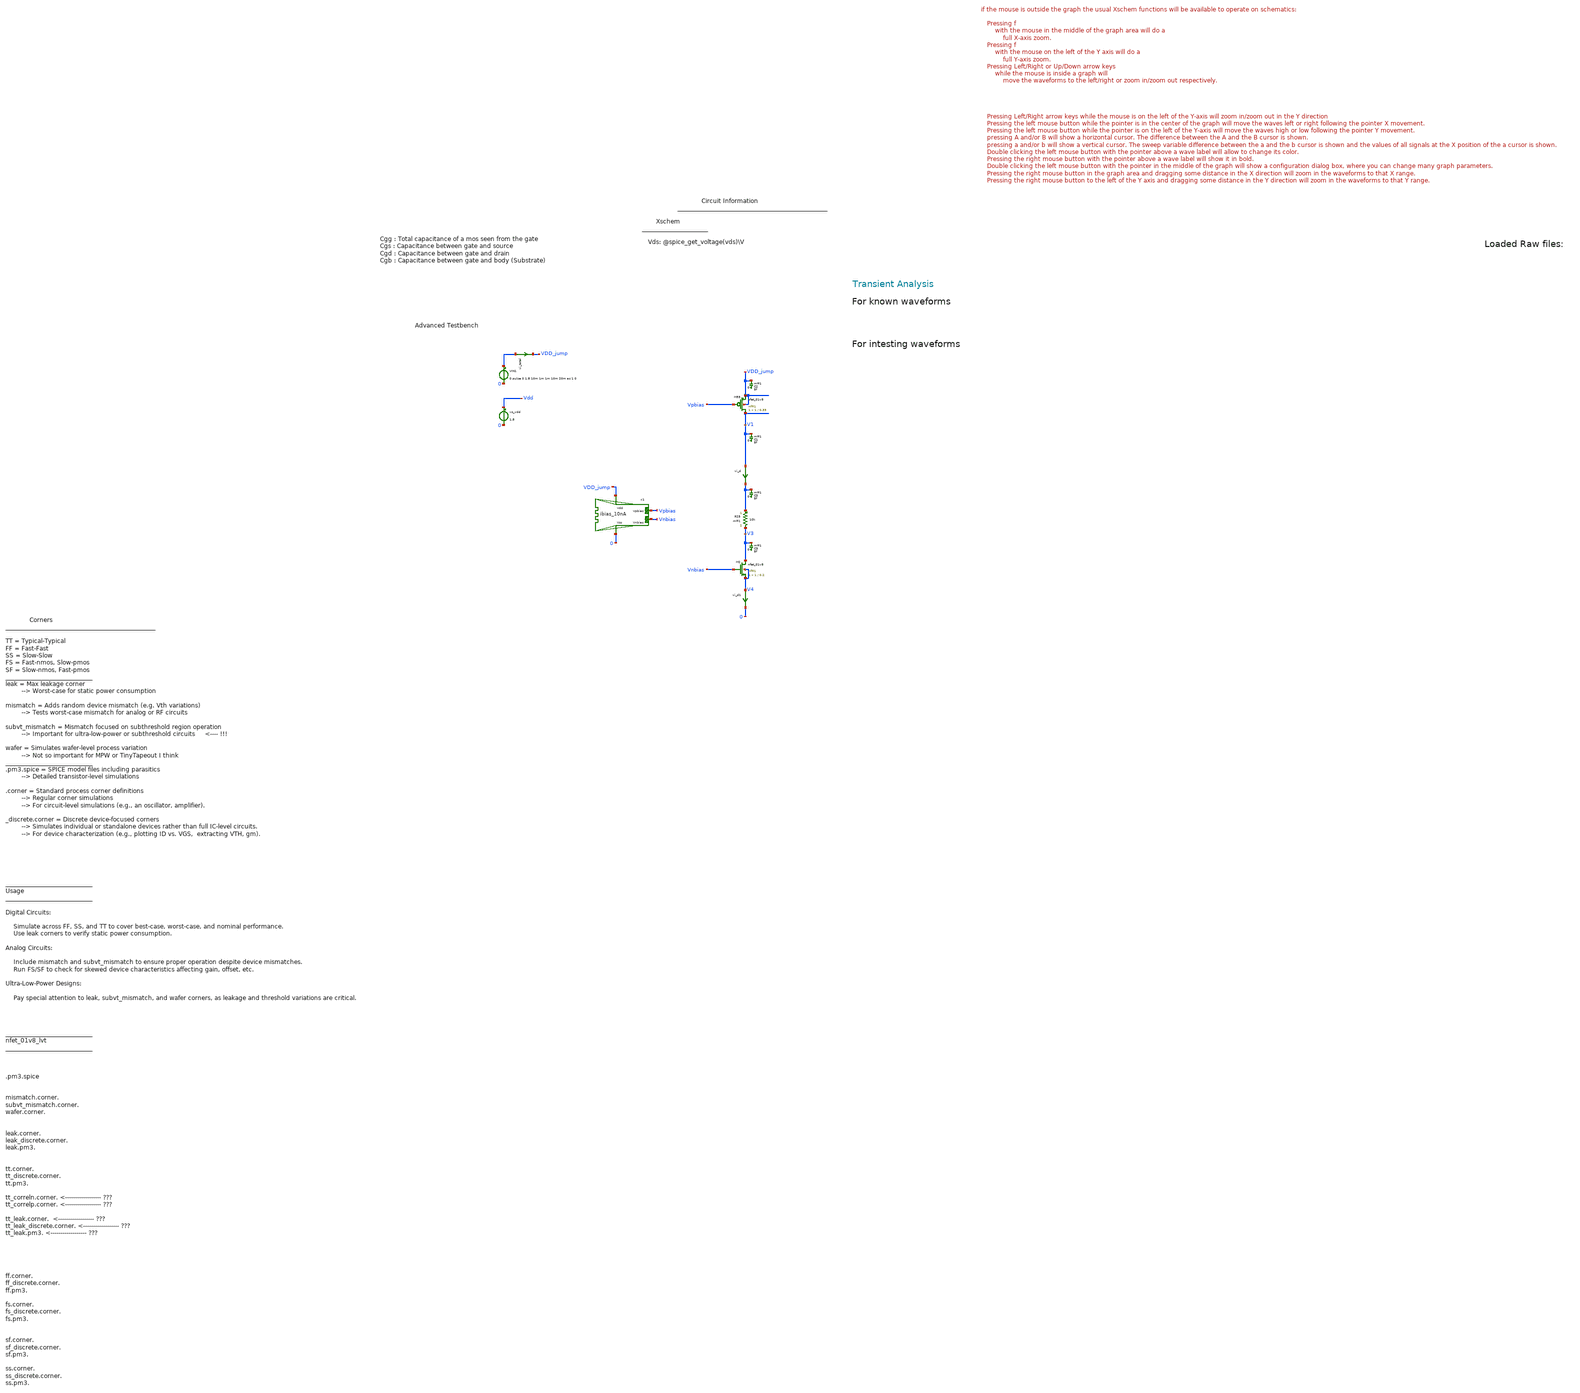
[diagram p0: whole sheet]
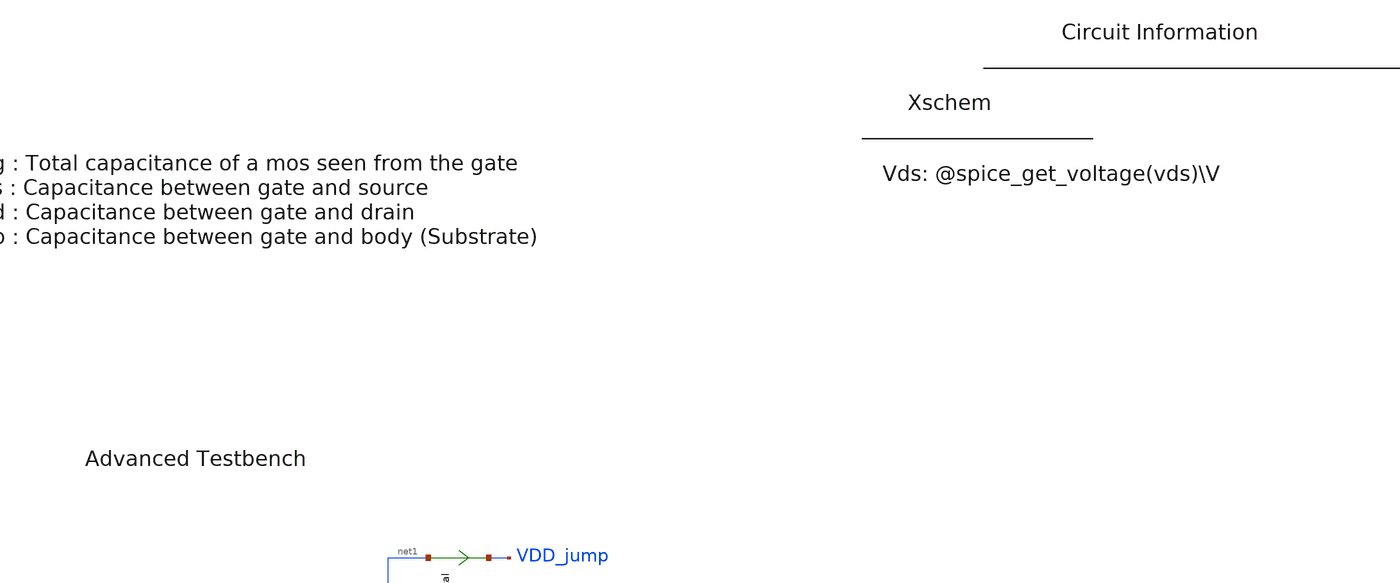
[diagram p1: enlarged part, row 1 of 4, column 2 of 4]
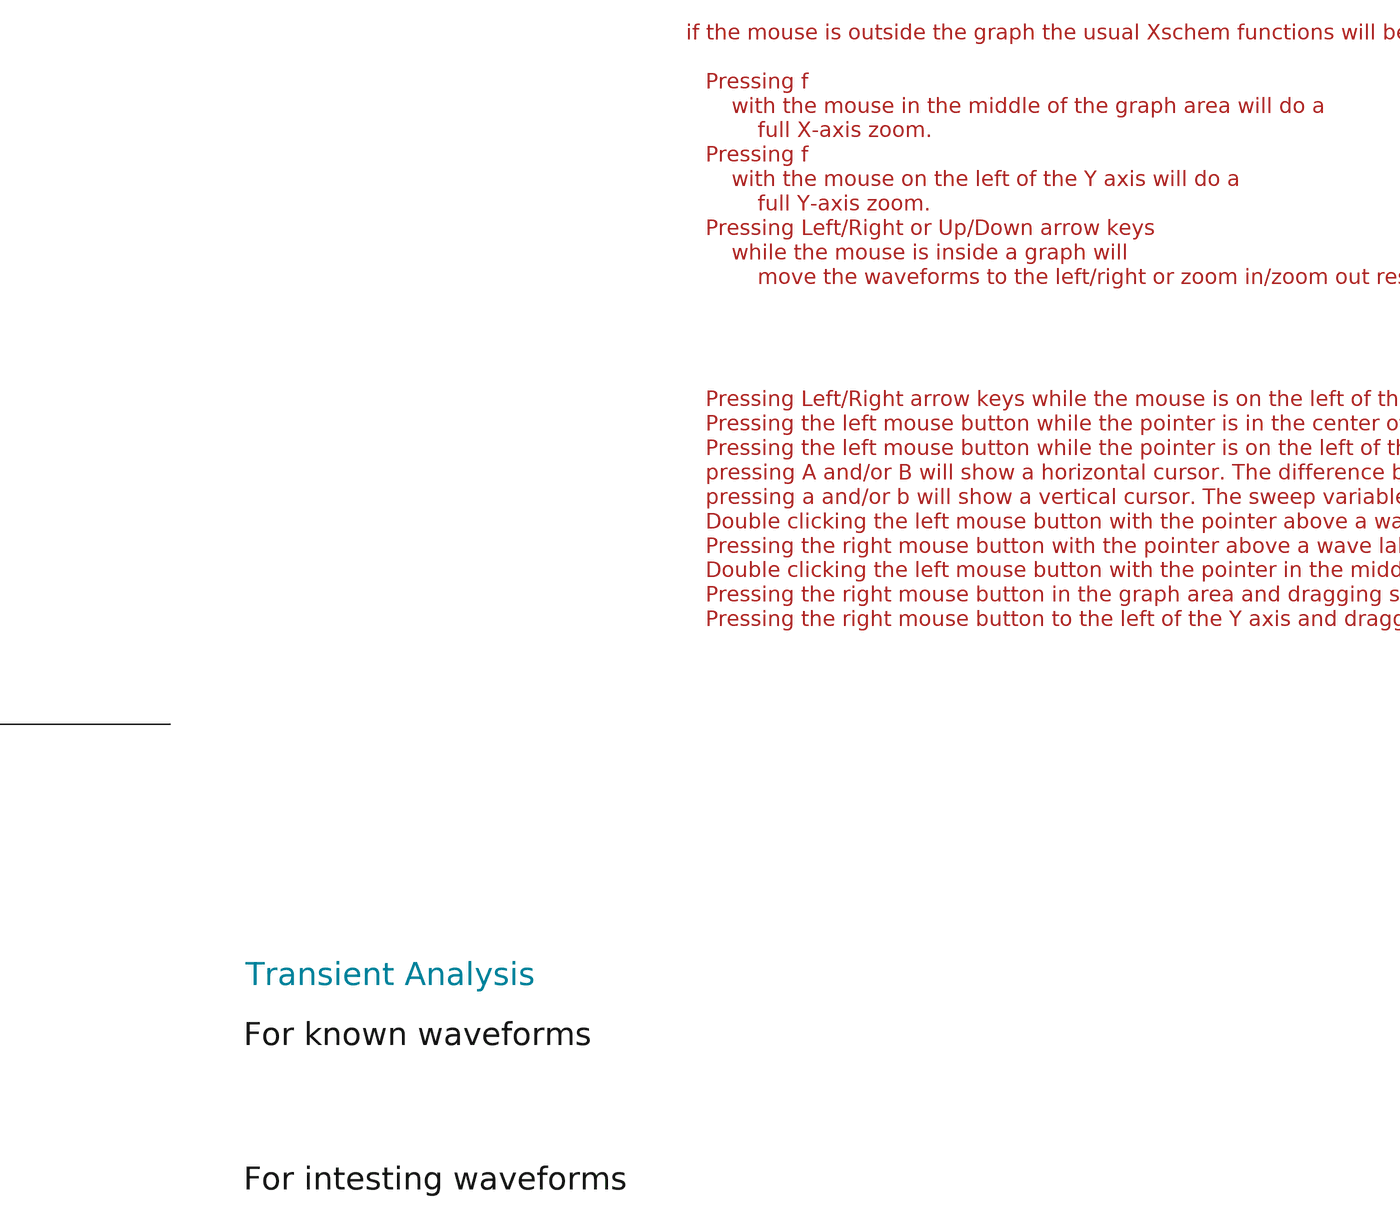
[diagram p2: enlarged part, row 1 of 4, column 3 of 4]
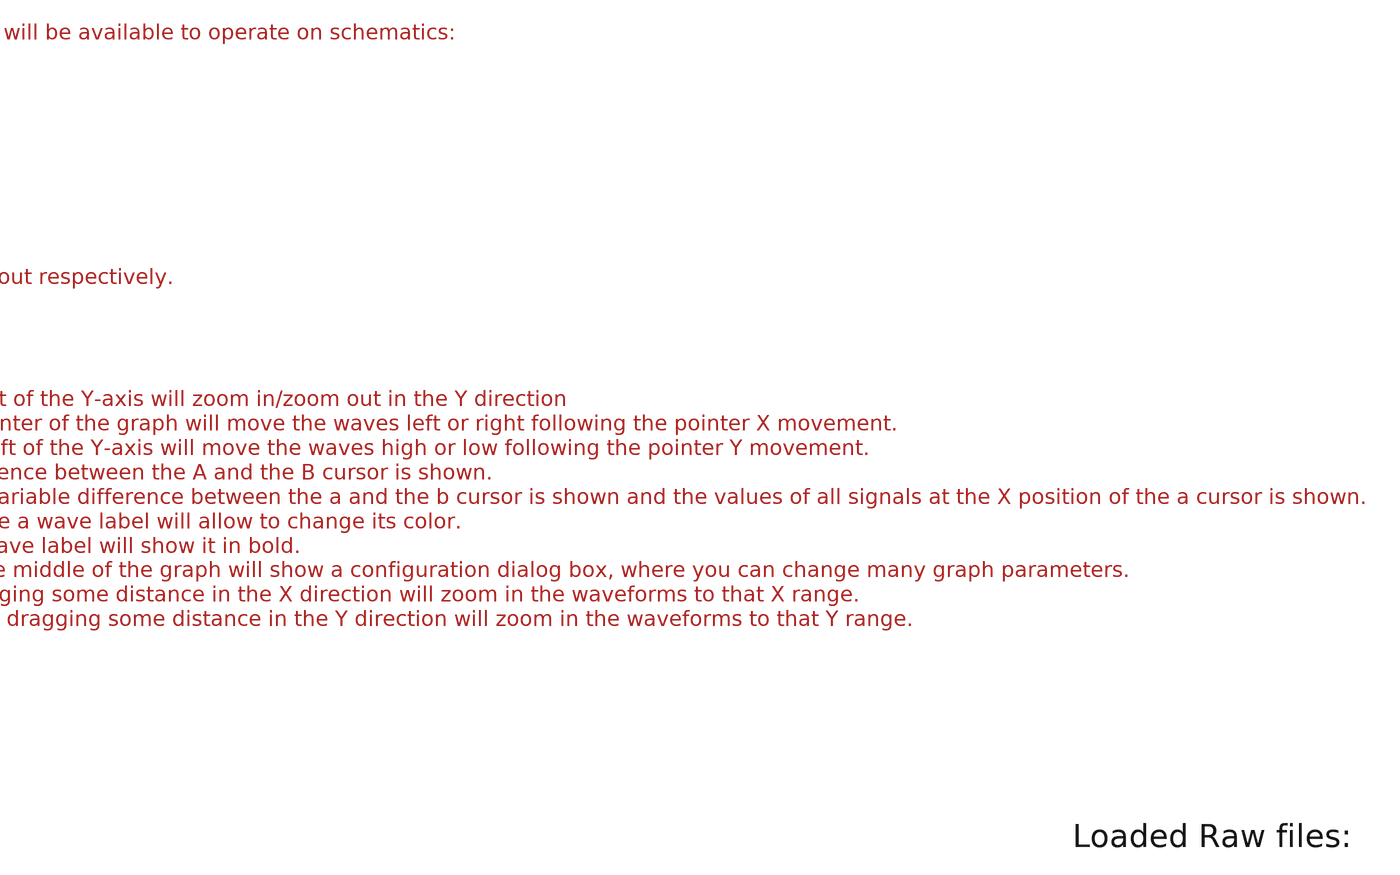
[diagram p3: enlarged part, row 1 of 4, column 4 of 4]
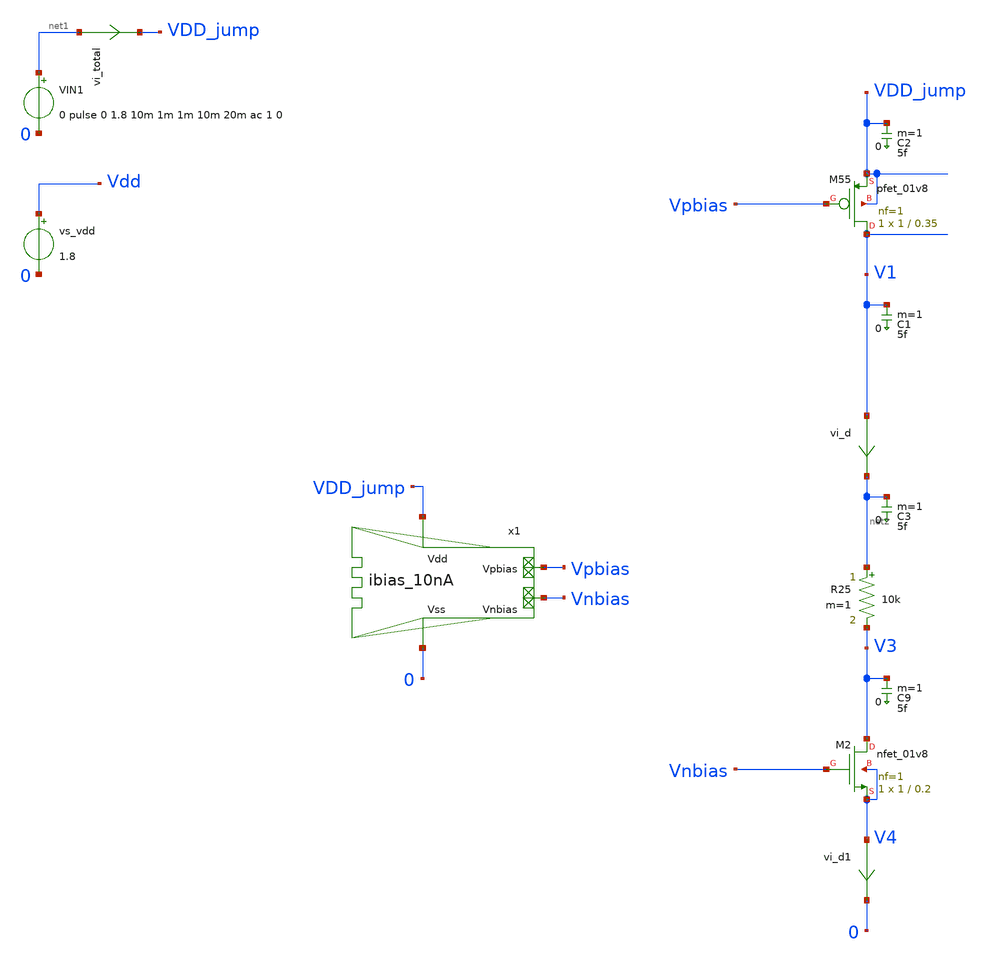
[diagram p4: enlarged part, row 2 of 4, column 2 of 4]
** sch_path: xschem/T2/biasGen/A_tt10_10nA/ibias_10nA__tran_tb.sch
* Copyright (C) 1998-2024 Stefan Frederik Schippers
* This program is free software; you can redistribute it and/or modify
* it under the terms of the GNU General Public License as published by
* the Free Software Foundation; either version 2 of the License, or
* (at your option) any later version.
* This program is distributed in the hope that it will be useful,
* but WITHOUT ANY WARRANTY; without even the implied warranty of
* MERCHANTABILITY or FITNESS FOR A PARTICULAR PURPOSE.  See the
* GNU General Public License for more details.
* You should have received a copy of the GNU General Public License
* along with this program; if not, write to the Free Software
**.subckt ibias_10nA__tran_tb
VIN1 net1 0 0 pulse 0 1.8 10m 1m 1m 10m 20m ac 1 0
vi_total net1 VDD_jump 0
.save i(vi_total)
vs_vdd Vdd 0 1.8
vi_d V1 net2 0
.save i(vi_d)
x1 VDD_jump 0 Vnbias Vpbias ibias_10nA
XM55 V1 Vpbias VDD_jump VDD_jump sky130_fd_pr__pfet_01v8 L=0.35 W=1 nf=1 ad='int((nf+1)/2) * W/nf * 0.29'
+ as='int((nf+2)/2) * W/nf * 0.29' pd='2*int((nf+1)/2) * (W/nf + 0.29)' ps='2*int((nf+2)/2) * (W/nf + 0.29)'
+ nrd='0.29 / W' nrs='0.29 / W' sa=0 sb=0 sd=0 mult=1 m=1
R25 net2 V3 10k m=1
C2 VDD_jump 0 5f m=1
C1 V1 0 5f m=1
C3 net2 0 5f m=1
XM2 V3 Vnbias V4 V4 sky130_fd_pr__nfet_01v8 L=0.2 W=1 nf=1 ad='int((1 + 1)/2) * 1 / 1 * 0.29' as='int((1 + 2)/2) * 1 / 1 * 0.29'
+ pd='2*int((1 + 1)/2) * (1 / 1 + 0.29)' ps='2*int((1 + 2)/2) * (1 / 1 + 0.29)' nrd='0.29 / 1 ' nrs='0.29 / 1 '
+ sa=0 sb=0 sd=0 mult=1 m=1
vi_d1 V4 0 0
.save i(vi_d1)
C9 V3 0 5f m=1
**** begin user architecture code



.temp 30

*.option gmin=5n
*.option scale=1e-6
.option wnflag=1
.option savecurrents

.save all
.control
  save all alli
  save @m.xm1.msky130_fd_pr__nfet_01v8[gm]
  save @m.xm1.msky130_fd_pr__nfet_01v8[id]
  save @m.xm1.msky130_fd_pr__nfet_01v8[vgs]

  save @m.xm1.msky130_fd_pr__nfet_01v8[cgg]
  save @m.xm1.msky130_fd_pr__nfet_01v8[cgs]
  save @m.xm1.msky130_fd_pr__nfet_01v8[cgdo]
  save @m.xm1.msky130_fd_pr__nfet_01v8[cgb]

  save @m.xm1.msky130_fd_pr__nfet_01v8[vds]
  save @m.xm1.msky130_fd_pr__nfet_01v8[vdsat]
  save @m.xm1.msky130_fd_pr__nfet_01v8[vth]


  save @m.xm1.msky130_fd_pr__nfet_01v8[leff]
  save @m.xm1.msky130_fd_pr__nfet_01v8[weff]
  save @m.xm1.msky130_fd_pr__nfet_01v8[gds]
  save @m.xm1.msky130_fd_pr__nfet_01v8[l]
  save @m.xm1.msky130_fd_pr__nfet_01v8[w]
  save @m.xm1.msky130_fd_pr__nfet_01v8[gm]
  save @m.xm1.msky130_fd_pr__nfet_01v8[gm]
  save @m.xm1.msky130_fd_pr__nfet_01v8[gm]
  save @m.xm1.msky130_fd_pr__nfet_01v8[gm]
  save @m.xm1.msky130_fd_pr__nfet_01v8[gm]








  tran 1m 50m
  remzerovec
  write nmos_tb_tran.raw

  op
  set appendwrite
  remzerovec
  write nmos_tb_tran.raw






  *quit 0




.endc





** opencircuitdesign pdks install
.lib $::SKYWATER_MODELS/sky130.lib.spice tt
.include $::SKYWATER_STDCELLS/sky130_fd_sc_hd.spice


**** end user architecture code
**.ends

* expanding   symbol:  T2/biasGen/A_tt10_10nA/ibias_10nA.sym # of pins=4
** sym_path: T2/biasGen/A_tt10_10nA/ibias_10nA.sym
** sch_path: T2/biasGen/A_tt10_10nA/ibias_10nA.sch
.subckt ibias_10nA Vdd Vss Vnbias Vpbias
*.ipin Vdd
*.ipin Vss
*.opin Vnbias
*.opin Vpbias
XM56 Vpbias Vpbias Vdd Vdd sky130_fd_pr__pfet_01v8 L=0.35 W=1 nf=1 ad='int((nf+1)/2) * W/nf * 0.29' as='int((nf+2)/2) * W/nf * 0.29'
+ pd='2*int((nf+1)/2) * (W/nf + 0.29)' ps='2*int((nf+2)/2) * (W/nf + 0.29)' nrd='0.29 / W' nrs='0.29 / W'
+ sa=0 sb=0 sd=0 mult=1 m=1
XM57 Vnbias Vpbias Vdd Vdd sky130_fd_pr__pfet_01v8 L=0.35 W=1 nf=1 ad='int((nf+1)/2) * W/nf * 0.29' as='int((nf+2)/2) * W/nf * 0.29'
+ pd='2*int((nf+1)/2) * (W/nf + 0.29)' ps='2*int((nf+2)/2) * (W/nf + 0.29)' nrd='0.29 / W' nrs='0.29 / W'
+ sa=0 sb=0 sd=0 mult=1 m=1
XM58 net2 Vpbias Vdd Vdd sky130_fd_pr__pfet_01v8 L=0.30 W=2 nf=1 ad='int((nf+1)/2) * W/nf * 0.29' as='int((nf+2)/2) * W/nf * 0.29'
+ pd='2*int((nf+1)/2) * (W/nf + 0.29)' ps='2*int((nf+2)/2) * (W/nf + 0.29)' nrd='0.29 / W' nrs='0.29 / W'
+ sa=0 sb=0 sd=0 mult=1 m=1
XM59 Vpbias Vnbias net1 net1 sky130_fd_pr__nfet_01v8 L=0.2 W=1 nf=1 ad='int((1 + 1)/2) * 1 / 1 * 0.29'
+ as='int((1 + 2)/2) * 1 / 1 * 0.29' pd='2*int((1 + 1)/2) * (1 / 1 + 0.29)' ps='2*int((1 + 2)/2) * (1 / 1 + 0.29)'
+ nrd='0.29 / 1 ' nrs='0.29 / 1 ' sa=0 sb=0 sd=0 mult=1 m=1
XM60 Vnbias Vnbias Vss Vss sky130_fd_pr__nfet_01v8 L=0.2 W=1 nf=1 ad='int((1 + 1)/2) * 1 / 1 * 0.29'
+ as='int((1 + 2)/2) * 1 / 1 * 0.29' pd='2*int((1 + 1)/2) * (1 / 1 + 0.29)' ps='2*int((1 + 2)/2) * (1 / 1 + 0.29)'
+ nrd='0.29 / 1 ' nrs='0.29 / 1 ' sa=0 sb=0 sd=0 mult=1 m=1
XM61 net2 net2 net1 net1 sky130_fd_pr__nfet_01v8 L=0.2 W=1 nf=1 ad='int((1 + 1)/2) * 1 / 1 * 0.29' as='int((1 + 2)/2) * 1 / 1 * 0.29'
+ pd='2*int((1 + 1)/2) * (1 / 1 + 0.29)' ps='2*int((1 + 2)/2) * (1 / 1 + 0.29)' nrd='0.29 / 1 ' nrs='0.29 / 1 '
+ sa=0 sb=0 sd=0 mult=1 m=1
XM62 net1 net2 Vss Vss sky130_fd_pr__nfet_01v8 L=1 W=1 nf=1 ad='int((1 + 1)/2) * 1 / 1 * 0.29' as='int((1 + 2)/2) * 1 / 1 * 0.29'
+ pd='2*int((1 + 1)/2) * (1 / 1 + 0.29)' ps='2*int((1 + 2)/2) * (1 / 1 + 0.29)' nrd='0.29 / 1 ' nrs='0.29 / 1 '
+ sa=0 sb=0 sd=0 mult=1 m=1
.ends

.end
